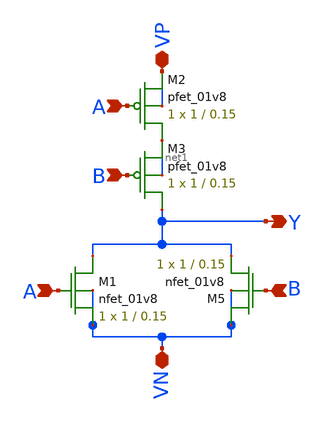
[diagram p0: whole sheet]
** sch_path: and/schematic/nand.sch
**.subckt nand B B VP VN A A Y
*.ipin B
*.ipin B
*.iopin VP
*.iopin VN
*.ipin A
*.ipin A
*.opin Y
XM1 Y A VN VN sky130_fd_pr__nfet_01v8 L=0.15 W=1 nf=1 ad='int((nf+1)/2) * W/nf * 0.29' as='int((nf+2)/2) * W/nf * 0.29'
+ pd='2*int((nf+1)/2) * (W/nf + 0.29)' ps='2*int((nf+2)/2) * (W/nf + 0.29)' nrd='0.29 / W' nrs='0.29 / W'
+ sa=0 sb=0 sd=0 mult=1 m=1
XM2 net1 A VP VP sky130_fd_pr__pfet_01v8 L=0.15 W=1 nf=1 ad='int((nf+1)/2) * W/nf * 0.29' as='int((nf+2)/2) * W/nf * 0.29'
+ pd='2*int((nf+1)/2) * (W/nf + 0.29)' ps='2*int((nf+2)/2) * (W/nf + 0.29)' nrd='0.29 / W' nrs='0.29 / W'
+ sa=0 sb=0 sd=0 mult=1 m=1
XM3 Y B net1 net1 sky130_fd_pr__pfet_01v8 L=0.15 W=1 nf=1 ad='int((nf+1)/2) * W/nf * 0.29' as='int((nf+2)/2) * W/nf * 0.29'
+ pd='2*int((nf+1)/2) * (W/nf + 0.29)' ps='2*int((nf+2)/2) * (W/nf + 0.29)' nrd='0.29 / W' nrs='0.29 / W'
+ sa=0 sb=0 sd=0 mult=1 m=1
XM5 VN B Y VN sky130_fd_pr__nfet_01v8 L=0.15 W=1 nf=1 ad='int((nf+1)/2) * W/nf * 0.29' as='int((nf+2)/2) * W/nf * 0.29'
+ pd='2*int((nf+1)/2) * (W/nf + 0.29)' ps='2*int((nf+2)/2) * (W/nf + 0.29)' nrd='0.29 / W' nrs='0.29 / W'
+ sa=0 sb=0 sd=0 mult=1 m=1
**.ends
.end
